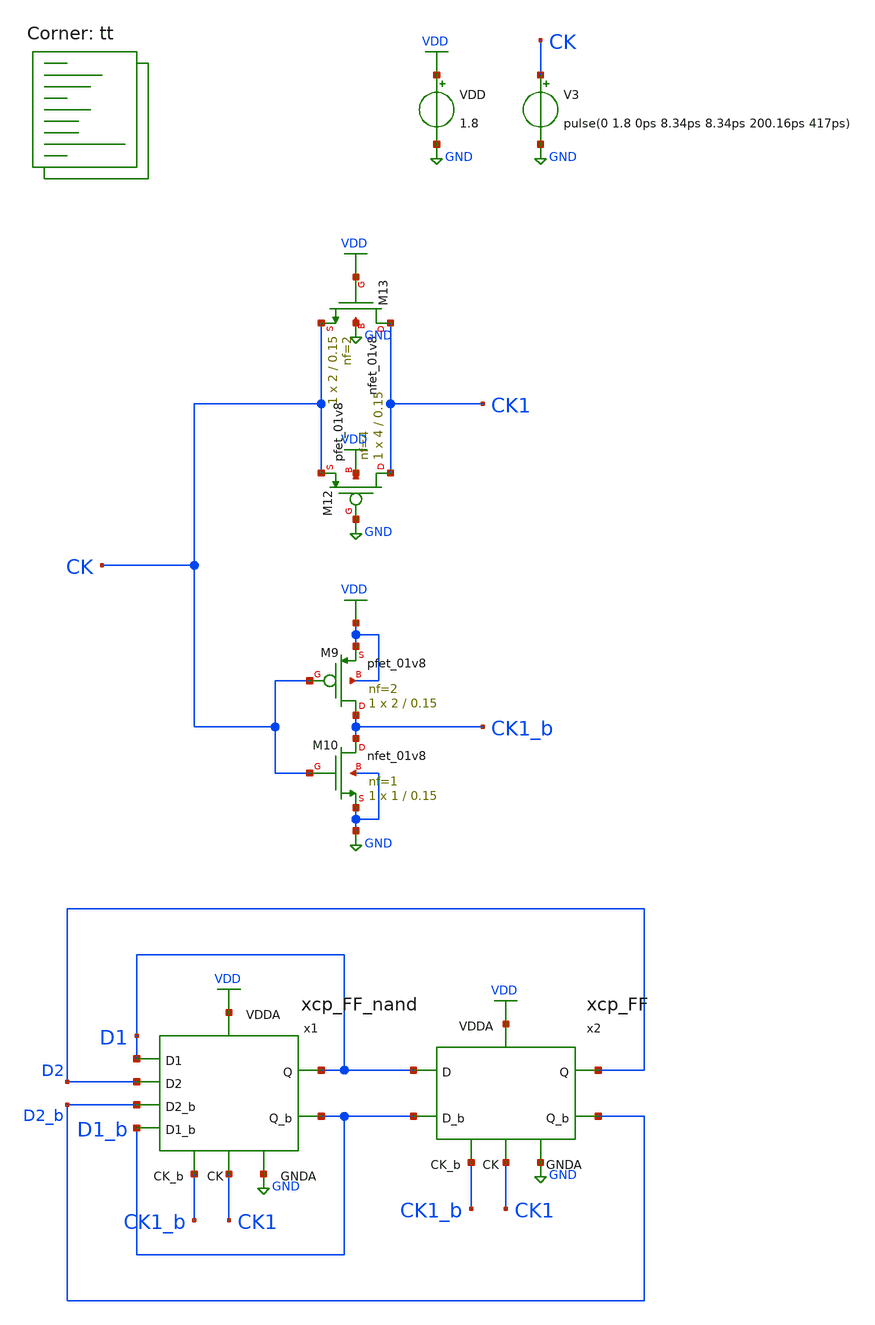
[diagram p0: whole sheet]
** sch_path: projects/pll/divider/xschem_ngspice/tb_xcp_FF_nand_divide3.sch
**.subckt tb_xcp_FF_nand_divide3
VDD VDD GND 1.8
V3 CK GND pulse(0 1.8 0ps 8.34ps 8.34ps 200.16ps 417ps)
XM12 CK1 GND CK VDD sky130_fd_pr__pfet_01v8 L=0.15 W=4 nf=4 ad='int((nf+1)/2) * W/nf * 0.29' as='int((nf+2)/2) * W/nf * 0.29'
+ pd='2*int((nf+1)/2) * (W/nf + 0.29)' ps='2*int((nf+2)/2) * (W/nf + 0.29)' nrd='0.29 / W' nrs='0.29 / W'
+ sa=0 sb=0 sd=0 mult=1 m=1
XM13 CK1 VDD CK GND sky130_fd_pr__nfet_01v8 L=0.15 W=2 nf=2 ad='int((nf+1)/2) * W/nf * 0.29' as='int((nf+2)/2) * W/nf * 0.29'
+ pd='2*int((nf+1)/2) * (W/nf + 0.29)' ps='2*int((nf+2)/2) * (W/nf + 0.29)' nrd='0.29 / W' nrs='0.29 / W'
+ sa=0 sb=0 sd=0 mult=1 m=1
XM9 CK1_b CK VDD VDD sky130_fd_pr__pfet_01v8 L=0.15 W=2 nf=2 ad='int((nf+1)/2) * W/nf * 0.29' as='int((nf+2)/2) * W/nf * 0.29'
+ pd='2*int((nf+1)/2) * (W/nf + 0.29)' ps='2*int((nf+2)/2) * (W/nf + 0.29)' nrd='0.29 / W' nrs='0.29 / W'
+ sa=0 sb=0 sd=0 mult=1 m=1
XM10 CK1_b CK GND GND sky130_fd_pr__nfet_01v8 L=0.15 W=1 nf=1 ad='int((nf+1)/2) * W/nf * 0.29' as='int((nf+2)/2) * W/nf * 0.29'
+ pd='2*int((nf+1)/2) * (W/nf + 0.29)' ps='2*int((nf+2)/2) * (W/nf + 0.29)' nrd='0.29 / W' nrs='0.29 / W'
+ sa=0 sb=0 sd=0 mult=1 m=1
x1 VDD D1 D1 D2 D2_b D1_b D1_b CK1_b CK1 GND xcp_FF_nand
x2 VDD D1 D2 D2_b D1_b CK1_b CK1 GND xcp_FF
**** begin user architecture code



.include /foss/pdks/sky130A/libs.ref/sky130_fd_sc_hd/spice/sky130_fd_sc_hd.spice

.option method=gear
.option wnflag=1
* .option savecurrents

.save @m.x1.xm1.msky130_fd_pr__nfet_01v8[gm] @m.x1.xm2.msky130_fd_pr__nfet_01v8[gm] @m.x1.xm3.msky130_fd_pr__pfet_01v8[gm] @m.x1.xm4.msky130_fd_pr__pfet_01v8[gm] @m.x1.xm5.msky130_fd_pr__nfet_01v8[gm] @m.x2.xm1.msky130_fd_pr__nfet_01v8[gm] @m.x2.xm2.msky130_fd_pr__nfet_01v8[gm] @m.x2.xm3.msky130_fd_pr__pfet_01v8[gm] @m.x2.xm4.msky130_fd_pr__pfet_01v8[gm] @m.x2.xm5.msky130_fd_pr__nfet_01v8[gm] @v.x1.vmeas @v.x1.vmeas1 @v.x1.vmeas2 @v.x5.vmeas @v.x5.vmeas1 @v.x5.vmeas2


*.ic v(b)=0

.control

  save v(d1) v(d1_b) v(d2) v(d2_b) v(q1) v(q1_b) v(ck) v(ck1) v(ck1_b)
  * save all
  *tran 0.1n 1u
  tran 0.2p 10n
  *ac dec 20 1 1T
  remzerovec
  write tb_xcp_FF_nand_divide3.raw

.endc



.lib $::SKYWATER_MODELS/sky130.lib.spice tt
**** end user architecture code
**.ends

* expanding   symbol:  /foss/designs/my_design/projects/pll/divider/xschem_ngspice/xcp_FF_nand.sym #
*+ of pins=10
** sym_path: projects/pll/divider/xschem_ngspice/xcp_FF_nand.sym
** sch_path: projects/pll/divider/xschem_ngspice/xcp_FF_nand.sch
.subckt xcp_FF_nand VDDA D1 Q D2 D2_b Q_b D1_b CK_b CK GNDA
*.ipin VDDA
*.opin Q
*.ipin CK
*.ipin GNDA
*.ipin D2
*.opin Q_b
*.ipin CK_b
*.ipin D2_b
*.ipin D1
*.ipin D1_b
x2 VDDA Q_b Q A_b A CK_b GNDA xcp_latch
x1 VDDA A_b A D1 D1_b D2_b D2 CK GNDA xcp_latch_nand
.ends


* expanding   symbol:  /foss/designs/my_design/projects/pll/divider/xschem_ngspice/xcp_FF.sym # of
*+ pins=8
** sym_path: projects/pll/divider/xschem_ngspice/xcp_FF.sym
** sch_path: projects/pll/divider/xschem_ngspice/xcp_FF.sch
.subckt xcp_FF VDDA D Q Q_b D_b CK_b CK GNDA
*.ipin VDDA
*.opin Q
*.ipin CK
*.ipin GNDA
*.opin Q_b
*.ipin CK_b
*.ipin D
*.ipin D_b
x2 VDDA Q_b Q A_b A CK_b GNDA xcp_latch
x1 VDDA A_b A D_b D CK GNDA xcp_latch
.ends


* expanding   symbol:  /foss/designs/my_design/projects/pll/divider/xschem_ngspice/xcp_latch.sym #
*+ of pins=7
** sym_path: projects/pll/divider/xschem_ngspice/xcp_latch.sym
** sch_path: projects/pll/divider/xschem_ngspice/xcp_latch.sch
.subckt xcp_latch VDDA Q_b Q D_b D CK GNDA
*.ipin D
*.opin Q
*.ipin D_b
*.ipin CK
*.opin Q_b
*.ipin VDDA
*.ipin GNDA
XM5 net1 CK GNDA GNDA sky130_fd_pr__nfet_01v8 L=0.15 W=2 nf=2 ad='int((nf+1)/2) * W/nf * 0.29' as='int((nf+2)/2) * W/nf * 0.29'
+ pd='2*int((nf+1)/2) * (W/nf + 0.29)' ps='2*int((nf+2)/2) * (W/nf + 0.29)' nrd='0.29 / W' nrs='0.29 / W'
+ sa=0 sb=0 sd=0 mult=1 m=1
XM1 net3 D V_common GNDA sky130_fd_pr__nfet_01v8 L=0.15 W=1 nf=1 ad='int((nf+1)/2) * W/nf * 0.29' as='int((nf+2)/2) * W/nf * 0.29'
+ pd='2*int((nf+1)/2) * (W/nf + 0.29)' ps='2*int((nf+2)/2) * (W/nf + 0.29)' nrd='0.29 / W' nrs='0.29 / W'
+ sa=0 sb=0 sd=0 mult=1 m=1
XM2 net2 D_b V_common GNDA sky130_fd_pr__nfet_01v8 L=0.15 W=1 nf=1 ad='int((nf+1)/2) * W/nf * 0.29' as='int((nf+2)/2) * W/nf * 0.29'
+ pd='2*int((nf+1)/2) * (W/nf + 0.29)' ps='2*int((nf+2)/2) * (W/nf + 0.29)' nrd='0.29 / W' nrs='0.29 / W'
+ sa=0 sb=0 sd=0 mult=1 m=1
Vmeas V_common net1 0
.save i(vmeas)
Vmeas1 Q_b net3 0
.save i(vmeas1)
Vmeas2 Q net2 0
.save i(vmeas2)
XM3 Q_b Q VDDA VDDA sky130_fd_pr__pfet_01v8 L=0.15 W=1 nf=1 ad='int((nf+1)/2) * W/nf * 0.29' as='int((nf+2)/2) * W/nf * 0.29'
+ pd='2*int((nf+1)/2) * (W/nf + 0.29)' ps='2*int((nf+2)/2) * (W/nf + 0.29)' nrd='0.29 / W' nrs='0.29 / W'
+ sa=0 sb=0 sd=0 mult=1 m=1
XM4 Q Q_b VDDA VDDA sky130_fd_pr__pfet_01v8 L=0.15 W=1 nf=1 ad='int((nf+1)/2) * W/nf * 0.29' as='int((nf+2)/2) * W/nf * 0.29'
+ pd='2*int((nf+1)/2) * (W/nf + 0.29)' ps='2*int((nf+2)/2) * (W/nf + 0.29)' nrd='0.29 / W' nrs='0.29 / W'
+ sa=0 sb=0 sd=0 mult=1 m=1
.ends


* expanding   symbol:
*+  /foss/designs/my_design/projects/pll/divider/xschem_ngspice/xcp_latch_nand.sym # of pins=9
** sym_path: projects/pll/divider/xschem_ngspice/xcp_latch_nand.sym
** sch_path: projects/pll/divider/xschem_ngspice/xcp_latch_nand.sch
.subckt xcp_latch_nand VDDA Q_b Q D1 D1_b D2_b D2 CK GNDA
*.ipin D2
*.opin Q
*.ipin D1_b
*.ipin CK
*.opin Q_b
*.ipin VDDA
*.ipin GNDA
*.ipin D1
*.ipin D2_b
XM5 net1 CK GNDA GNDA sky130_fd_pr__nfet_01v8 L=0.15 W=2 nf=2 ad='int((nf+1)/2) * W/nf * 0.29' as='int((nf+2)/2) * W/nf * 0.29'
+ pd='2*int((nf+1)/2) * (W/nf + 0.29)' ps='2*int((nf+2)/2) * (W/nf + 0.29)' nrd='0.29 / W' nrs='0.29 / W'
+ sa=0 sb=0 sd=0 mult=1 m=1
XM1 net4 D2 V_common GNDA sky130_fd_pr__nfet_01v8 L=0.15 W=1 nf=1 ad='int((nf+1)/2) * W/nf * 0.29' as='int((nf+2)/2) * W/nf * 0.29'
+ pd='2*int((nf+1)/2) * (W/nf + 0.29)' ps='2*int((nf+2)/2) * (W/nf + 0.29)' nrd='0.29 / W' nrs='0.29 / W'
+ sa=0 sb=0 sd=0 mult=1 m=1
XM2 net2 D1_b V_common GNDA sky130_fd_pr__nfet_01v8 L=0.15 W=1 nf=1 ad='int((nf+1)/2) * W/nf * 0.29'
+ as='int((nf+2)/2) * W/nf * 0.29' pd='2*int((nf+1)/2) * (W/nf + 0.29)' ps='2*int((nf+2)/2) * (W/nf + 0.29)'
+ nrd='0.29 / W' nrs='0.29 / W' sa=0 sb=0 sd=0 mult=1 m=1
Vmeas V_common net1 0
.save i(vmeas)
Vmeas1 Q_b net3 0
.save i(vmeas1)
Vmeas2 Q net2 0
.save i(vmeas2)
XM3 Q_b Q VDDA VDDA sky130_fd_pr__pfet_01v8 L=0.15 W=1 nf=1 ad='int((nf+1)/2) * W/nf * 0.29' as='int((nf+2)/2) * W/nf * 0.29'
+ pd='2*int((nf+1)/2) * (W/nf + 0.29)' ps='2*int((nf+2)/2) * (W/nf + 0.29)' nrd='0.29 / W' nrs='0.29 / W'
+ sa=0 sb=0 sd=0 mult=1 m=1
XM4 Q Q_b VDDA VDDA sky130_fd_pr__pfet_01v8 L=0.15 W=1 nf=1 ad='int((nf+1)/2) * W/nf * 0.29' as='int((nf+2)/2) * W/nf * 0.29'
+ pd='2*int((nf+1)/2) * (W/nf + 0.29)' ps='2*int((nf+2)/2) * (W/nf + 0.29)' nrd='0.29 / W' nrs='0.29 / W'
+ sa=0 sb=0 sd=0 mult=1 m=1
XM6 net3 D1 net4 GNDA sky130_fd_pr__nfet_01v8 L=0.15 W=1 nf=1 ad='int((nf+1)/2) * W/nf * 0.29' as='int((nf+2)/2) * W/nf * 0.29'
+ pd='2*int((nf+1)/2) * (W/nf + 0.29)' ps='2*int((nf+2)/2) * (W/nf + 0.29)' nrd='0.29 / W' nrs='0.29 / W'
+ sa=0 sb=0 sd=0 mult=1 m=1
XM7 net2 D2_b V_common GNDA sky130_fd_pr__nfet_01v8 L=0.15 W=1 nf=1 ad='int((nf+1)/2) * W/nf * 0.29'
+ as='int((nf+2)/2) * W/nf * 0.29' pd='2*int((nf+1)/2) * (W/nf + 0.29)' ps='2*int((nf+2)/2) * (W/nf + 0.29)'
+ nrd='0.29 / W' nrs='0.29 / W' sa=0 sb=0 sd=0 mult=1 m=1
.ends

.GLOBAL GND
.GLOBAL VDD
.end
